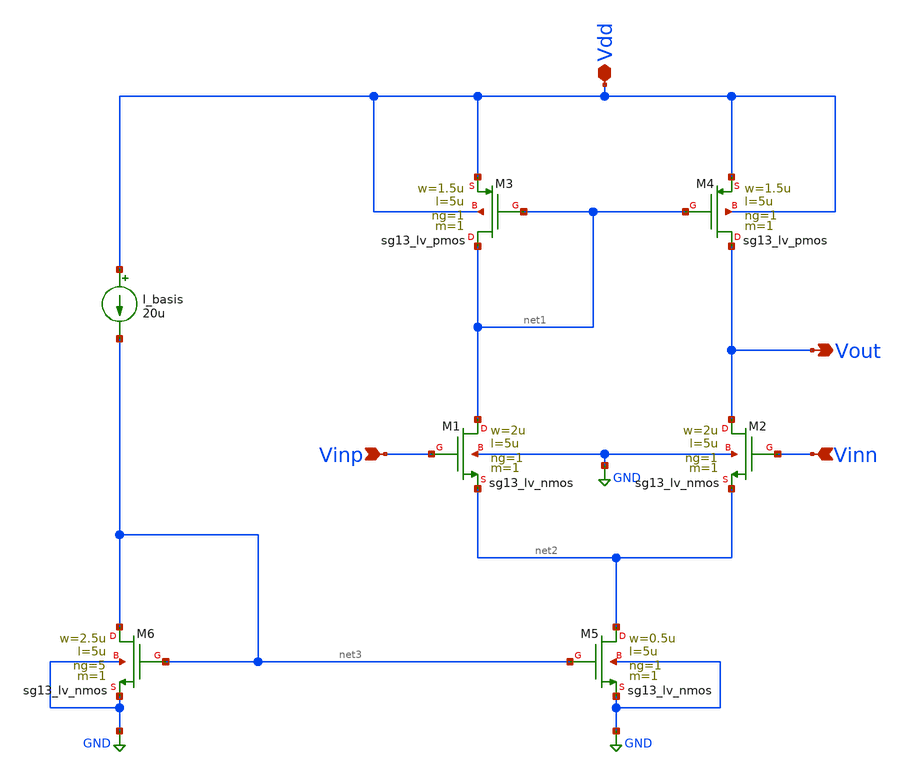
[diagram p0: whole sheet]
** sch_path: Xschem/OTA_test.sch
**.subckt OTA_test Vout Vdd Vinp Vinn
*.opin Vout
*.iopin Vdd
*.ipin Vinp
*.ipin Vinn
I_basis Vdd net3 20u
XM1 net1 Vinp net2 GND sg13_lv_nmos w=2u l=5u ng=1 m=1 mm_ok=1
XM5 net2 net3 GND GND sg13_lv_nmos w=0.5u l=5u ng=1 m=1 mm_ok=1
XM6 net3 net3 GND GND sg13_lv_nmos w=2.5u l=5u ng=5 m=1 mm_ok=1
XM4 Vout net1 Vdd Vdd sg13_lv_pmos w=1.5u l=5u ng=1 m=1 mm_ok=1
XM3 net1 net1 Vdd Vdd sg13_lv_pmos w=1.5u l=5u ng=1 m=1 mm_ok=1
XM2 Vout Vinn net2 GND sg13_lv_nmos w=2u l=5u ng=1 m=1 mm_ok=1
**.ends
.GLOBAL GND
.end
